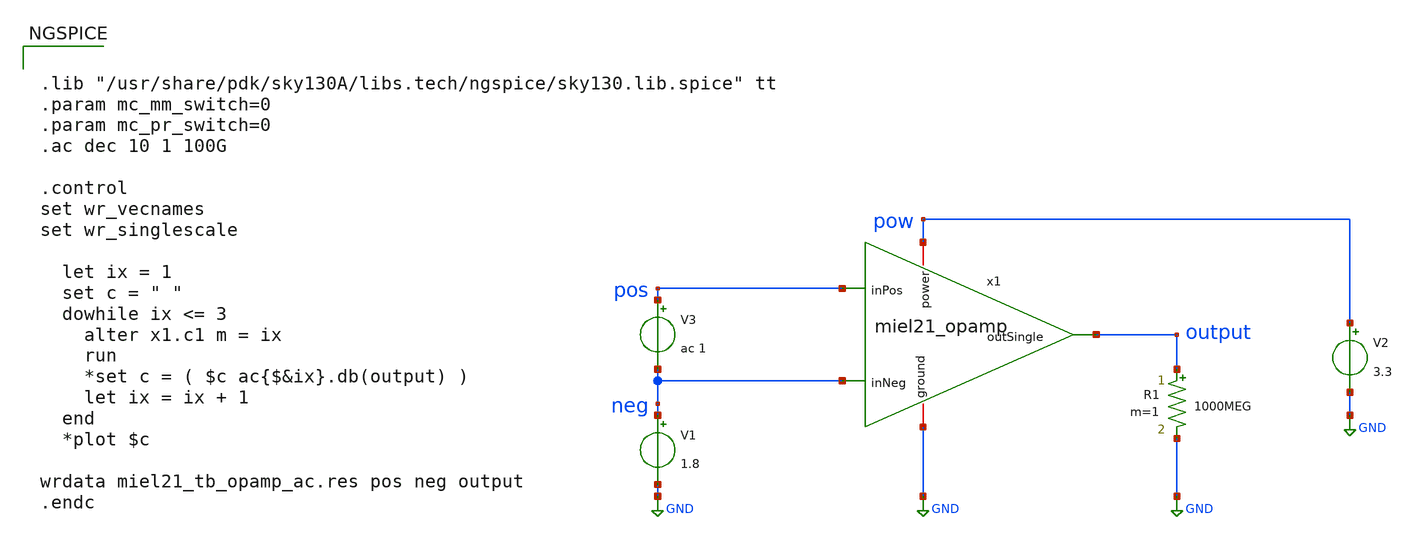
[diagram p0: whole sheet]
** sch_path: dev/opamp/miel21_tb_opamp_ac_param_CC.sch
**.subckt miel21_tb_opamp_ac_param_CC
V1 neg GND 1.8
V2 pow GND 3.3
R1 output GND 1000MEG m=1
V3 pos neg ac 1
x1 pow output pos neg GND miel21_opamp
**** begin user architecture code


.lib "/usr/share/pdk/sky130A/libs.tech/ngspice/sky130.lib.spice" tt
.param mc_mm_switch=0
.param mc_pr_switch=0
.ac dec 10 1 100G

.control
set wr_vecnames
set wr_singlescale

  let ix = 1
  set c = " "
  dowhile ix <= 3
    alter x1.c1 m = ix
    run
    *set c = ( $c ac{$&ix}.db(output) )
    let ix = ix + 1
  end
  *plot $c

wrdata miel21_tb_opamp_ac.res pos neg output
.endc


**** end user architecture code
**.ends

* expanding   symbol:  miel21_opamp.sym # of pins=5
** sym_path: dev/opamp/miel21_opamp.sym
** sch_path: dev/opamp/miel21_opamp.sch
.subckt miel21_opamp power outSingle inPos inNeg ground
*.ipin inPos
*.ipin inNeg
*.opin outSingle
*.iopin power
*.iopin ground
XM6 d1 d1 power power sky130_fd_pr__pfet_g5v0d10v5 L=0.5 W=21 nf=3 ad='int((nf+1)/2) * W/nf * 0.29' as='int((nf+2)/2) * W/nf * 0.29'
+ pd='2*int((nf+1)/2) * (W/nf + 0.29)' ps='2*int((nf+2)/2) * (W/nf + 0.29)' nrd='0.29 / W' nrs='0.29 / W'
+ sa=0 sb=0 sd=0 mult=1 m=1
XM7 d2 d1 power power sky130_fd_pr__pfet_g5v0d10v5 L=0.5 W=21 nf=3 ad='int((nf+1)/2) * W/nf * 0.29' as='int((nf+2)/2) * W/nf * 0.29'
+ pd='2*int((nf+1)/2) * (W/nf + 0.29)' ps='2*int((nf+2)/2) * (W/nf + 0.29)' nrd='0.29 / W' nrs='0.29 / W'
+ sa=0 sb=0 sd=0 mult=1 m=1
XM8 outSingle d2 power power sky130_fd_pr__pfet_g5v0d10v5 L=0.5 W=260 nf=20 ad='int((nf+1)/2) * W/nf * 0.29'
+ as='int((nf+2)/2) * W/nf * 0.29' pd='2*int((nf+1)/2) * (W/nf + 0.29)' ps='2*int((nf+2)/2) * (W/nf + 0.29)'
+ nrd='0.29 / W' nrs='0.29 / W' sa=0 sb=0 sd=0 mult=1 m=1
XM1 d1 inPos nsources ground sky130_fd_pr__nfet_g5v0d10v5 L=0.5 W=5 nf=1 ad='int((nf+1)/2) * W/nf * 0.29'
+ as='int((nf+2)/2) * W/nf * 0.29' pd='2*int((nf+1)/2) * (W/nf + 0.29)' ps='2*int((nf+2)/2) * (W/nf + 0.29)'
+ nrd='0.29 / W' nrs='0.29 / W' sa=0 sb=0 sd=0 mult=1 m=1
XM2 d2 inNeg nsources ground sky130_fd_pr__nfet_g5v0d10v5 L=0.5 W=5 nf=1 ad='int((nf+1)/2) * W/nf * 0.29'
+ as='int((nf+2)/2) * W/nf * 0.29' pd='2*int((nf+1)/2) * (W/nf + 0.29)' ps='2*int((nf+2)/2) * (W/nf + 0.29)'
+ nrd='0.29 / W' nrs='0.29 / W' sa=0 sb=0 sd=0 mult=1 m=1
XM3 bias bias ground ground sky130_fd_pr__nfet_g5v0d10v5 L=0.5 W=10 nf=2 ad='int((nf+1)/2) * W/nf * 0.29'
+ as='int((nf+2)/2) * W/nf * 0.29' pd='2*int((nf+1)/2) * (W/nf + 0.29)' ps='2*int((nf+2)/2) * (W/nf + 0.29)'
+ nrd='0.29 / W' nrs='0.29 / W' sa=0 sb=0 sd=0 mult=1 m=1
XM4 nsources bias ground ground sky130_fd_pr__nfet_g5v0d10v5 L=0.5 W=10 nf=2 ad='int((nf+1)/2) * W/nf * 0.29'
+ as='int((nf+2)/2) * W/nf * 0.29' pd='2*int((nf+1)/2) * (W/nf + 0.29)' ps='2*int((nf+2)/2) * (W/nf + 0.29)'
+ nrd='0.29 / W' nrs='0.29 / W' sa=0 sb=0 sd=0 mult=1 m=1
XM5 outSingle bias ground ground sky130_fd_pr__nfet_g5v0d10v5 L=0.5 W=48 nf=8 ad='int((nf+1)/2) * W/nf * 0.29'
+ as='int((nf+2)/2) * W/nf * 0.29' pd='2*int((nf+1)/2) * (W/nf + 0.29)' ps='2*int((nf+2)/2) * (W/nf + 0.29)'
+ nrd='0.29 / W' nrs='0.29 / W' sa=0 sb=0 sd=0 mult=1 m=1
XR1 bias net2 ground sky130_fd_pr__res_xhigh_po_0p69 L=6 mult=1 m=1
XC1 outSingle d2 sky130_fd_pr__cap_mim_m3_1 W=10 L=14 MF=1 m=1
XR2 net2 net1 ground sky130_fd_pr__res_xhigh_po_0p69 L=6 mult=1 m=1
XR3 net1 power ground sky130_fd_pr__res_xhigh_po_0p69 L=6 mult=1 m=1
.ends

.GLOBAL GND
.end
